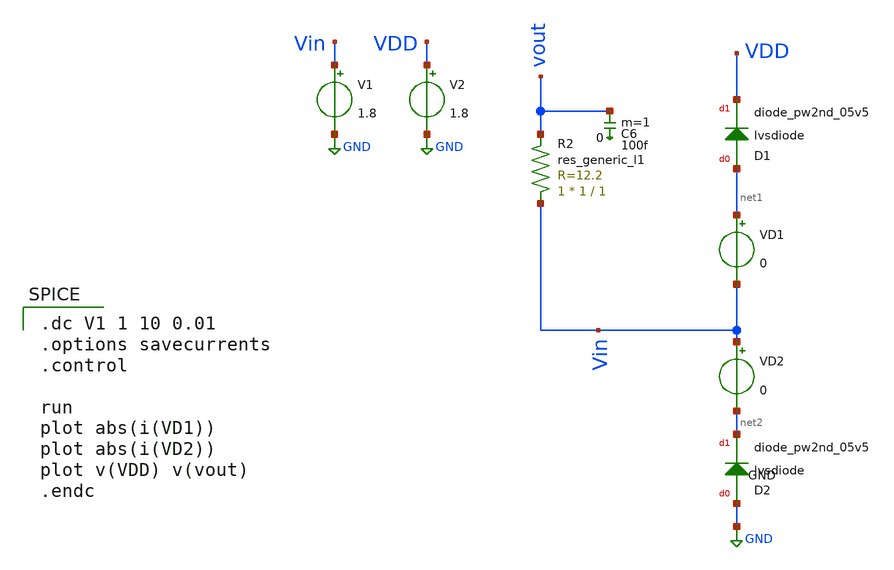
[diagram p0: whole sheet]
** sch_path: sky130_cells/ESD_Diode/TB_Flatten.sch
**.subckt TB_Flatten
D1 net1 VDD sky130_fd_pr__diode_pw2nd_05v5 area=1e12
D2 GND net2 sky130_fd_pr__diode_pw2nd_05v5 area=1e12
R2 Vin vout sky130_fd_pr__res_generic_l1 W=1 L=1 m=1
VD1 net1 Vin 0
V1 Vin GND 1.8
V2 VDD GND 1.8
C6 vout 0 100f m=1
VD2 Vin net2 0
**** begin user architecture code
 .lib /usr/local/share/pdk/sky130A/libs.tech/ngspice/sky130.lib.spice tt

.dc V1 1 10 0.01
.options savecurrents
.control

run
plot abs(i(VD1))
plot abs(i(VD2))
plot v(VDD) v(vout)
.endc

**** end user architecture code
**.ends
.GLOBAL GND
.end
